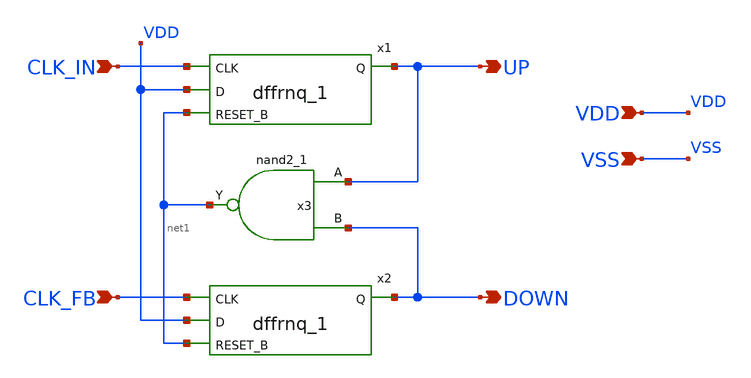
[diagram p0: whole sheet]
** sch_path: designs/libs/core_analog/pfd/pfd.sch
**.subckt pfd UP DOWN CLK_IN CLK_FB VDD VSS
*.opin UP
*.opin DOWN
*.ipin CLK_IN
*.ipin CLK_FB
*.ipin VDD
*.ipin VSS
x1 VDD net1 CLK_IN UP VDD VDD VSS VSS gf180mcu_fd_sc_mcu7t5v0__dffrnq_1
x2 VDD net1 CLK_FB DOWN VDD VDD VSS VSS gf180mcu_fd_sc_mcu7t5v0__dffrnq_1
x3 UP DOWN net1 VDD VDD VSS VSS gf180mcu_fd_sc_mcu7t5v0__nand2_1
**.ends
.end
